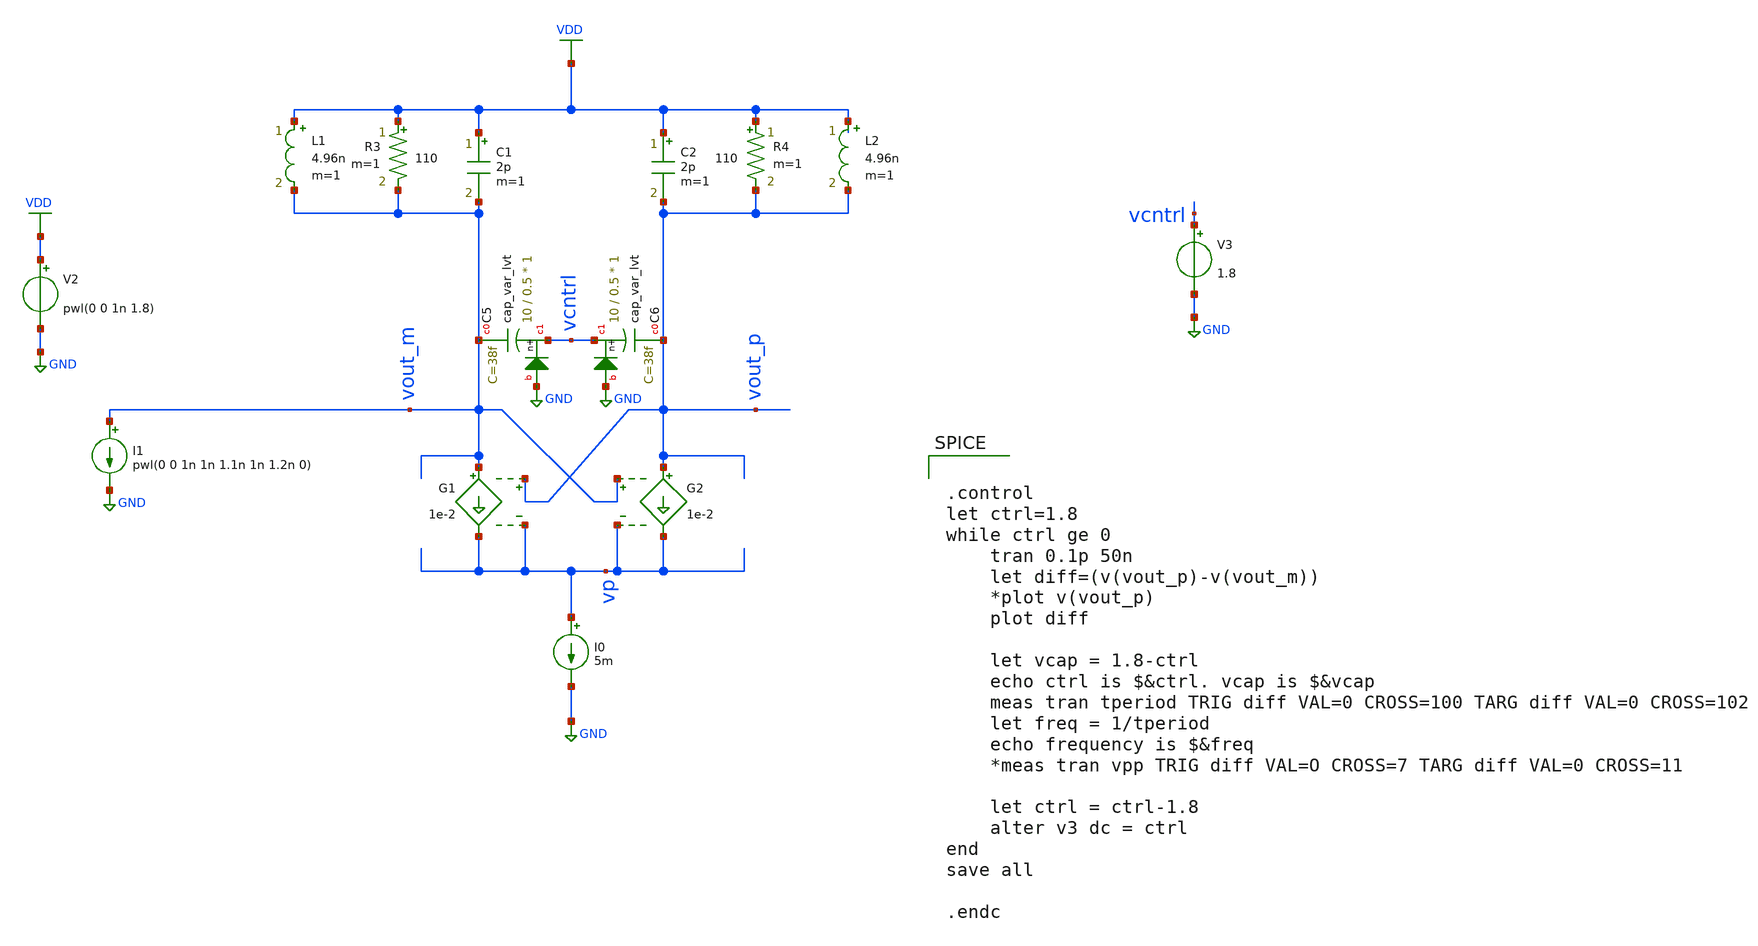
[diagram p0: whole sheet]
** sch_path: vco_vccs_with_var.sch
**.subckt vco_vccs_with_var
I0 vp GND 5m
G1 vout_m vp vout_p vp 1e-2
G2 vout_p vp vout_m vp 1e-2
R3 VDD vout_m 110 m=1
R4 VDD vout_p 110 m=1
L1 VDD vout_m 4.96n m=1
L2 VDD vout_p 4.96n m=1
V2 VDD GND pwl(0 0 1n 1.8)
V3 vcntrl GND 1.8
XC5 vout_m vcntrl GND sky130_fd_pr__cap_var_lvt W=10 L=0.5 VM=1 m=1
XC6 vout_p vcntrl GND sky130_fd_pr__cap_var_lvt W=10 L=0.5 VM=1 m=1
C1 VDD vout_m 2p m=1
C2 VDD vout_p 2p m=1
I1 vout_m GND pwl(0 0 1n 1n 1.1n 1n 1.2n 0)
**** begin user architecture code


.option wnflag = 1
.lib /usr/local/share/pdk/sky130A/libs.tech/ngspice/sky130.lib.spice tt
.include /usr/local/share/pdk/sky130A/libs.ref/sky130_fd_pr/spice/sky130_fd_pr__ind_05_220.model.spice
.param mc_mm_switch=0




.control
let ctrl=1.8
while ctrl ge 0
	tran 0.1p 50n
	let diff=(v(vout_p)-v(vout_m))
	*plot v(vout_p)
	plot diff

	let vcap = 1.8-ctrl
	echo ctrl is $&ctrl. vcap is $&vcap
	meas tran tperiod TRIG diff VAL=0 CROSS=100 TARG diff VAL=0 CROSS=102
	let freq = 1/tperiod
	echo frequency is $&freq
	*meas tran vpp TRIG diff VAL=O CROSS=7 TARG diff VAL=0 CROSS=11

	let ctrl = ctrl-1.8
	alter v3 dc = ctrl
end
save all

.endc


**** end user architecture code
**.ends
.GLOBAL VDD
.GLOBAL GND
.end
